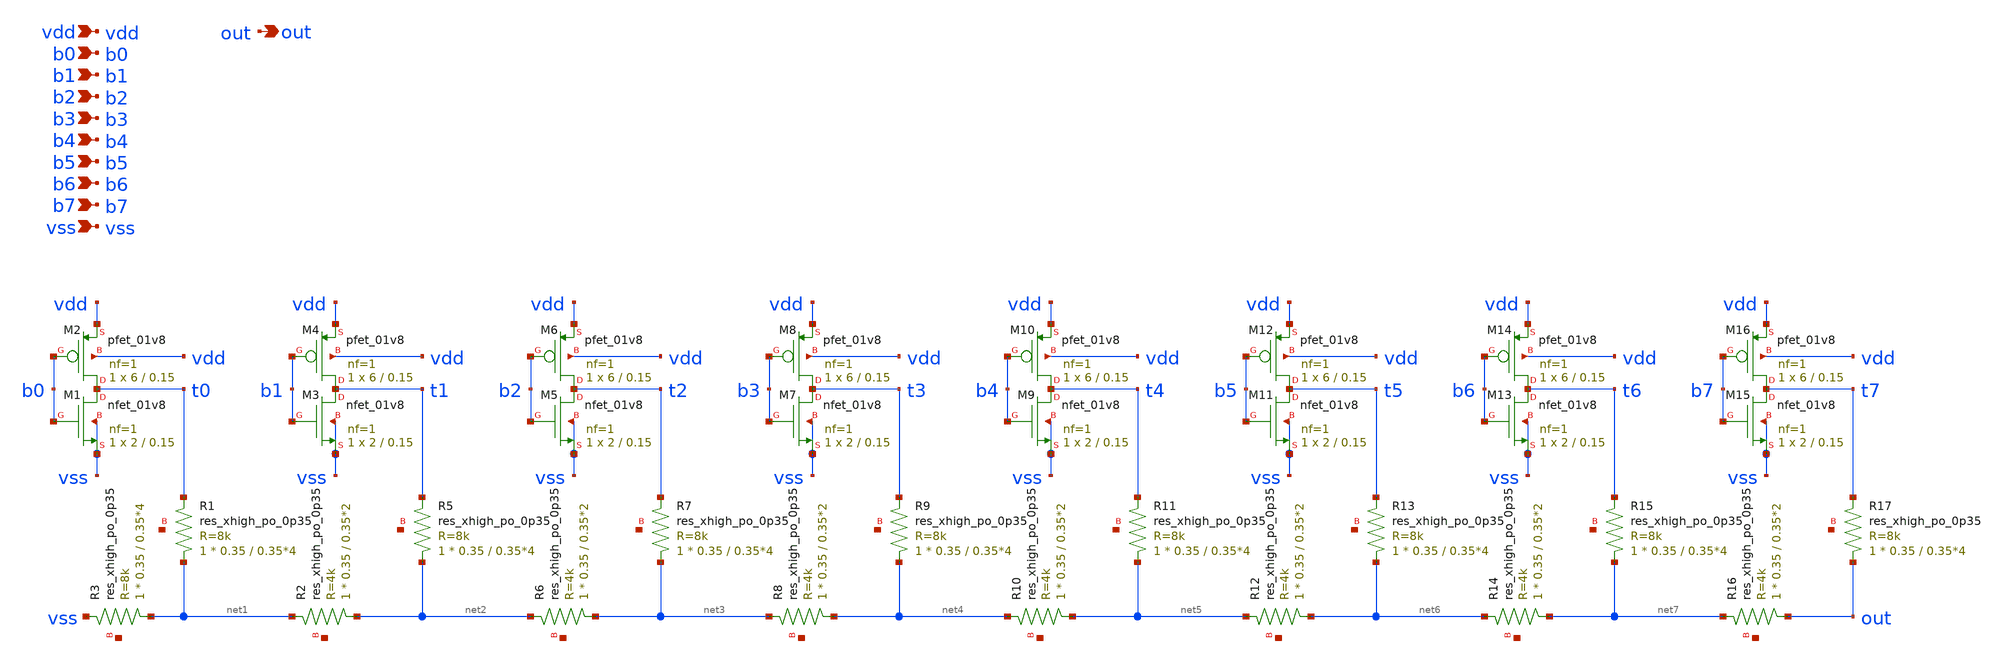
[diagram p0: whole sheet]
** sch_path: custom_gds/tt_um_tim2305_adc_dac/xschem/r2r_dac.sch
**.subckt r2r_dac vdd out b0 b1 b2 b3 b4 b5 b6 b7 vss
*.ipin vdd
*.opin out
*.ipin b0
*.ipin b1
*.ipin b2
*.ipin b3
*.ipin b4
*.ipin b5
*.ipin b6
*.ipin b7
*.ipin vss
XR3 net1 vss net8 sky130_fd_pr__res_xhigh_po_0p35 L=0.35*4 mult=1 m=1
XR1 net1 t0 net9 sky130_fd_pr__res_xhigh_po_0p35 L=0.35*4 mult=1 m=1
XR2 net2 net1 net10 sky130_fd_pr__res_xhigh_po_0p35 L=0.35*2 mult=1 m=1
XR5 net2 t1 net11 sky130_fd_pr__res_xhigh_po_0p35 L=0.35*4 mult=1 m=1
XR6 net3 net2 net12 sky130_fd_pr__res_xhigh_po_0p35 L=0.35*2 mult=1 m=1
XR7 net3 t2 net13 sky130_fd_pr__res_xhigh_po_0p35 L=0.35*4 mult=1 m=1
XR8 net4 net3 net14 sky130_fd_pr__res_xhigh_po_0p35 L=0.35*2 mult=1 m=1
XR9 net4 t3 net15 sky130_fd_pr__res_xhigh_po_0p35 L=0.35*4 mult=1 m=1
XR10 net5 net4 net16 sky130_fd_pr__res_xhigh_po_0p35 L=0.35*2 mult=1 m=1
XR11 net5 t4 net17 sky130_fd_pr__res_xhigh_po_0p35 L=0.35*4 mult=1 m=1
XR12 net6 net5 net18 sky130_fd_pr__res_xhigh_po_0p35 L=0.35*2 mult=1 m=1
XR13 net6 t5 net19 sky130_fd_pr__res_xhigh_po_0p35 L=0.35*4 mult=1 m=1
XR14 net7 net6 net20 sky130_fd_pr__res_xhigh_po_0p35 L=0.35*2 mult=1 m=1
XR15 net7 t6 net21 sky130_fd_pr__res_xhigh_po_0p35 L=0.35*4 mult=1 m=1
XR16 out net7 net22 sky130_fd_pr__res_xhigh_po_0p35 L=0.35*2 mult=1 m=1
XR17 out t7 net23 sky130_fd_pr__res_xhigh_po_0p35 L=0.35*4 mult=1 m=1
XM2 t0 b0 vdd vdd sky130_fd_pr__pfet_01v8 L=0.15 W=6 nf=1 ad='int((nf+1)/2) * W/nf * 0.29' as='int((nf+2)/2) * W/nf * 0.29'
+ pd='2*int((nf+1)/2) * (W/nf + 0.29)' ps='2*int((nf+2)/2) * (W/nf + 0.29)' nrd='0.29 / W' nrs='0.29 / W'
+ sa=0 sb=0 sd=0 mult=1 m=1
XM4 t1 b1 vdd vdd sky130_fd_pr__pfet_01v8 L=0.15 W=6 nf=1 ad='int((nf+1)/2) * W/nf * 0.29' as='int((nf+2)/2) * W/nf * 0.29'
+ pd='2*int((nf+1)/2) * (W/nf + 0.29)' ps='2*int((nf+2)/2) * (W/nf + 0.29)' nrd='0.29 / W' nrs='0.29 / W'
+ sa=0 sb=0 sd=0 mult=1 m=1
XM6 t2 b2 vdd vdd sky130_fd_pr__pfet_01v8 L=0.15 W=6 nf=1 ad='int((nf+1)/2) * W/nf * 0.29' as='int((nf+2)/2) * W/nf * 0.29'
+ pd='2*int((nf+1)/2) * (W/nf + 0.29)' ps='2*int((nf+2)/2) * (W/nf + 0.29)' nrd='0.29 / W' nrs='0.29 / W'
+ sa=0 sb=0 sd=0 mult=1 m=1
XM8 t3 b3 vdd vdd sky130_fd_pr__pfet_01v8 L=0.15 W=6 nf=1 ad='int((nf+1)/2) * W/nf * 0.29' as='int((nf+2)/2) * W/nf * 0.29'
+ pd='2*int((nf+1)/2) * (W/nf + 0.29)' ps='2*int((nf+2)/2) * (W/nf + 0.29)' nrd='0.29 / W' nrs='0.29 / W'
+ sa=0 sb=0 sd=0 mult=1 m=1
XM10 t4 b4 vdd vdd sky130_fd_pr__pfet_01v8 L=0.15 W=6 nf=1 ad='int((nf+1)/2) * W/nf * 0.29' as='int((nf+2)/2) * W/nf * 0.29'
+ pd='2*int((nf+1)/2) * (W/nf + 0.29)' ps='2*int((nf+2)/2) * (W/nf + 0.29)' nrd='0.29 / W' nrs='0.29 / W'
+ sa=0 sb=0 sd=0 mult=1 m=1
XM12 t5 b5 vdd vdd sky130_fd_pr__pfet_01v8 L=0.15 W=6 nf=1 ad='int((nf+1)/2) * W/nf * 0.29' as='int((nf+2)/2) * W/nf * 0.29'
+ pd='2*int((nf+1)/2) * (W/nf + 0.29)' ps='2*int((nf+2)/2) * (W/nf + 0.29)' nrd='0.29 / W' nrs='0.29 / W'
+ sa=0 sb=0 sd=0 mult=1 m=1
XM14 t6 b6 vdd vdd sky130_fd_pr__pfet_01v8 L=0.15 W=6 nf=1 ad='int((nf+1)/2) * W/nf * 0.29' as='int((nf+2)/2) * W/nf * 0.29'
+ pd='2*int((nf+1)/2) * (W/nf + 0.29)' ps='2*int((nf+2)/2) * (W/nf + 0.29)' nrd='0.29 / W' nrs='0.29 / W'
+ sa=0 sb=0 sd=0 mult=1 m=1
XM16 t7 b7 vdd vdd sky130_fd_pr__pfet_01v8 L=0.15 W=6 nf=1 ad='int((nf+1)/2) * W/nf * 0.29' as='int((nf+2)/2) * W/nf * 0.29'
+ pd='2*int((nf+1)/2) * (W/nf + 0.29)' ps='2*int((nf+2)/2) * (W/nf + 0.29)' nrd='0.29 / W' nrs='0.29 / W'
+ sa=0 sb=0 sd=0 mult=1 m=1
XM1 t0 b0 vss vss sky130_fd_pr__nfet_01v8 L=0.15 W=2 nf=1 ad='int((nf+1)/2) * W/nf * 0.29' as='int((nf+2)/2) * W/nf * 0.29'
+ pd='2*int((nf+1)/2) * (W/nf + 0.29)' ps='2*int((nf+2)/2) * (W/nf + 0.29)' nrd='0.29 / W' nrs='0.29 / W'
+ sa=0 sb=0 sd=0 mult=1 m=1
XM3 t1 b1 vss vss sky130_fd_pr__nfet_01v8 L=0.15 W=2 nf=1 ad='int((nf+1)/2) * W/nf * 0.29' as='int((nf+2)/2) * W/nf * 0.29'
+ pd='2*int((nf+1)/2) * (W/nf + 0.29)' ps='2*int((nf+2)/2) * (W/nf + 0.29)' nrd='0.29 / W' nrs='0.29 / W'
+ sa=0 sb=0 sd=0 mult=1 m=1
XM5 t2 b2 vss vss sky130_fd_pr__nfet_01v8 L=0.15 W=2 nf=1 ad='int((nf+1)/2) * W/nf * 0.29' as='int((nf+2)/2) * W/nf * 0.29'
+ pd='2*int((nf+1)/2) * (W/nf + 0.29)' ps='2*int((nf+2)/2) * (W/nf + 0.29)' nrd='0.29 / W' nrs='0.29 / W'
+ sa=0 sb=0 sd=0 mult=1 m=1
XM7 t3 b3 vss vss sky130_fd_pr__nfet_01v8 L=0.15 W=2 nf=1 ad='int((nf+1)/2) * W/nf * 0.29' as='int((nf+2)/2) * W/nf * 0.29'
+ pd='2*int((nf+1)/2) * (W/nf + 0.29)' ps='2*int((nf+2)/2) * (W/nf + 0.29)' nrd='0.29 / W' nrs='0.29 / W'
+ sa=0 sb=0 sd=0 mult=1 m=1
XM9 t4 b4 vss vss sky130_fd_pr__nfet_01v8 L=0.15 W=2 nf=1 ad='int((nf+1)/2) * W/nf * 0.29' as='int((nf+2)/2) * W/nf * 0.29'
+ pd='2*int((nf+1)/2) * (W/nf + 0.29)' ps='2*int((nf+2)/2) * (W/nf + 0.29)' nrd='0.29 / W' nrs='0.29 / W'
+ sa=0 sb=0 sd=0 mult=1 m=1
XM11 t5 b5 vss vss sky130_fd_pr__nfet_01v8 L=0.15 W=2 nf=1 ad='int((nf+1)/2) * W/nf * 0.29' as='int((nf+2)/2) * W/nf * 0.29'
+ pd='2*int((nf+1)/2) * (W/nf + 0.29)' ps='2*int((nf+2)/2) * (W/nf + 0.29)' nrd='0.29 / W' nrs='0.29 / W'
+ sa=0 sb=0 sd=0 mult=1 m=1
XM13 t6 b6 vss vss sky130_fd_pr__nfet_01v8 L=0.15 W=2 nf=1 ad='int((nf+1)/2) * W/nf * 0.29' as='int((nf+2)/2) * W/nf * 0.29'
+ pd='2*int((nf+1)/2) * (W/nf + 0.29)' ps='2*int((nf+2)/2) * (W/nf + 0.29)' nrd='0.29 / W' nrs='0.29 / W'
+ sa=0 sb=0 sd=0 mult=1 m=1
XM15 t7 b7 vss vss sky130_fd_pr__nfet_01v8 L=0.15 W=2 nf=1 ad='int((nf+1)/2) * W/nf * 0.29' as='int((nf+2)/2) * W/nf * 0.29'
+ pd='2*int((nf+1)/2) * (W/nf + 0.29)' ps='2*int((nf+2)/2) * (W/nf + 0.29)' nrd='0.29 / W' nrs='0.29 / W'
+ sa=0 sb=0 sd=0 mult=1 m=1
**.ends
.end
